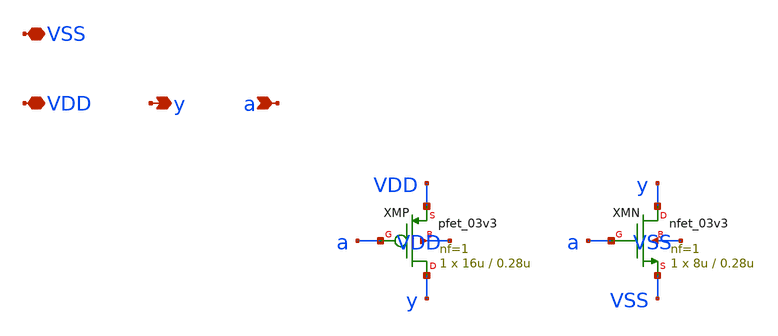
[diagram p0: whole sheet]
** sch_path: design/inv_x16.sch
**.subckt inv_x16 a y VDD VSS
*.ipin a
*.opin y
*.iopin VDD
*.iopin VSS
XMP y a VDD VDD pfet_03v3 L=0.28u W=16u nf=1 ad='int((nf+1)/2) * W/nf * 0.18u' as='int((nf+2)/2) * W/nf * 0.18u'
+ pd='2*int((nf+1)/2) * (W/nf + 0.18u)' ps='2*int((nf+2)/2) * (W/nf + 0.18u)' nrd='0.18u / W' nrs='0.18u / W'
+ sa=0 sb=0 sd=0 m=1
XMN y a VSS VSS nfet_03v3 L=0.28u W=8u nf=1 ad='int((nf+1)/2) * W/nf * 0.18u' as='int((nf+2)/2) * W/nf * 0.18u'
+ pd='2*int((nf+1)/2) * (W/nf + 0.18u)' ps='2*int((nf+2)/2) * (W/nf + 0.18u)' nrd='0.18u / W' nrs='0.18u / W'
+ sa=0 sb=0 sd=0 m=1
**.ends
.end
